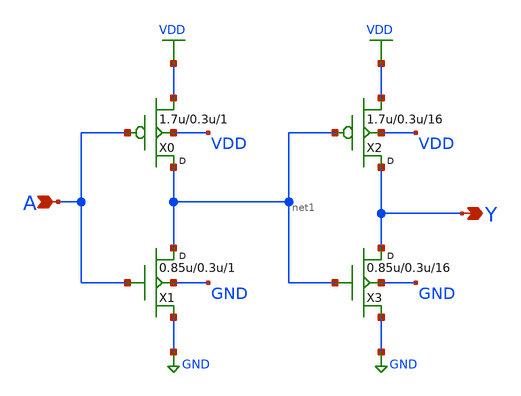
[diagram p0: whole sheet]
** sch_path: gf180mcu_osu_sc_gp9t3v3/cells/clkbuf/gf180mcu_osu_sc_gp9t3v3__clkbuf_16.sch
**.subckt gf180mcu_osu_sc_gp9t3v3__clkbuf_16 A Y
*.ipin A
*.opin Y
X0 net1 A VDD VDD pfet_03p3 w=1.7u l=0.3u m=1
X1 net1 A GND GND nfet_03p3 w=0.85u l=0.3u m=1
X2 Y net1 VDD VDD pfet_03p3 w=1.7u l=0.3u m=16
X3 Y net1 GND GND nfet_03p3 w=0.85u l=0.3u m=16
**.ends
.GLOBAL VDD
.GLOBAL GND
.end
